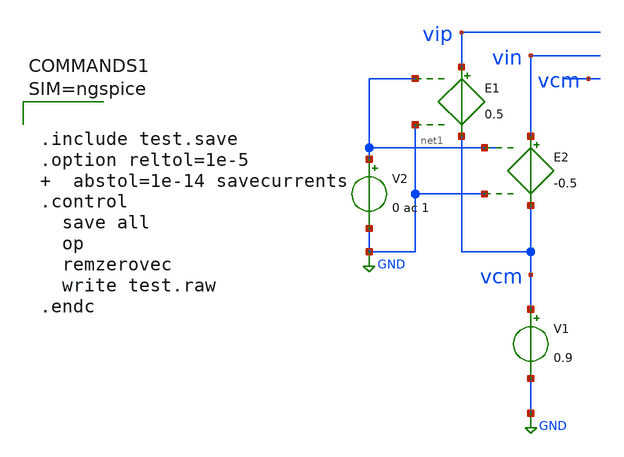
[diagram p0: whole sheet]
** sch_path: test.sch
**.subckt test
E1 vip vcm net1 GND 0.5
E2 vin vcm net1 GND -0.5
V1 vcm GND 0.9
V2 net1 GND 0 ac 1
**** begin user architecture code



.include test.save
.option reltol=1e-5   abstol=1e-14 savecurrents
.control
  save all
  op
  remzerovec
  write test.raw
.endc



**** end user architecture code
**.ends
.GLOBAL GND
.end
